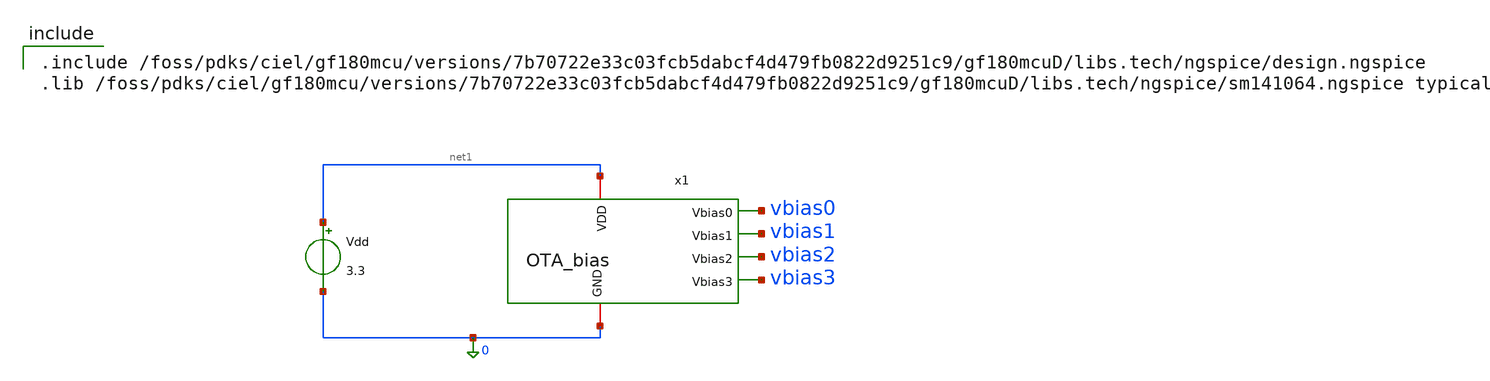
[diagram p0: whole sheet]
** sch_path: analog/tb_OTA_bias.sch
**.subckt tb_OTA_bias
x1 net1 vbias0 vbias2 vbias3 vbias1 0 OTA_bias cur_factor=1
Vdd net1 0 3.3
**** begin user architecture code

.include /foss/pdks/ciel/gf180mcu/versions/7b70722e33c03fcb5dabcf4d479fb0822d9251c9/gf180mcuD/libs.tech/ngspice/design.ngspice
.lib /foss/pdks/ciel/gf180mcu/versions/7b70722e33c03fcb5dabcf4d479fb0822d9251c9/gf180mcuD/libs.tech/ngspice/sm141064.ngspice typical



.control
alter @m.x1.x1.xm6.m0[w] = 10u

dc Vdd 0 3.3 0.05

plot (v(vbias0) - v(vbias3)) v(vbias1) v(vbias2)
plot @m.x1.x1.x1.xm6.m0[id] @m.x1.x1.x1.xm7.m0[id]
plot @m.x1.x1.xm2.m0[id] @m.x1.x1.xm6.m0[id] @m.x1.x1.xm9.m0[id] @m.x1.x1.xm1.m0[id]
+ @m.x1.x1.xm5.m0[id] @m.x1.x1.xm3.m0[id]

op
print @m.x1.x1.xm2.m0[id]
print @m.x1.x1.xm6.m0[id]
print @m.x1.x1.xm9.m0[id]
print @m.x1.x1.xm1.m0[id]
print @m.x1.x1.xm5.m0[id]
print @m.x1.x1.xm3.m0[id]
.endc


**** end user architecture code
**.ends

* expanding   symbol:
*+  AURA-Event-Driven-Mixed-Signal-ASIC-for-Acoustic-Pattern-Detection/analog/OTA_bias.sym # of pins=6
** sym_path: analog/OTA_bias.sym
** sch_path: analog/OTA_bias.sch
.subckt OTA_bias VDD Vbias0 Vbias2 Vbias3 Vbias1 GND  cur_factor=1
*.iopin VDD
*.opin Vbias2
*.opin Vbias1
*.opin Vbias0
*.opin Vbias3
*.iopin GND
XM1 Vbias1 GND Vbias2 VDD pfet_03v3 L=4u W=5u nf=1 ad='int((nf+1)/2) * W/nf * 0.18u' as='int((nf+2)/2) * W/nf * 0.18u'
+ pd='2*int((nf+1)/2) * (W/nf + 0.18u)' ps='2*int((nf+2)/2) * (W/nf + 0.18u)' nrd='0.18u / W' nrs='0.18u / W'
+ sa=0 sb=0 sd=0 m=1
XM4 Vbias1 Vbias2 net1 GND nfet_03v3 L=4u W=1u nf=1 ad='int((nf+1)/2) * W/nf * 0.18u' as='int((nf+2)/2) * W/nf * 0.18u'
+ pd='2*int((nf+1)/2) * (W/nf + 0.18u)' ps='2*int((nf+2)/2) * (W/nf + 0.18u)' nrd='0.18u / W' nrs='0.18u / W'
+ sa=0 sb=0 sd=0 m=1
XM5 net1 Vbias1 GND GND nfet_03v3 L=4u W=1u nf=1 ad='int((nf+1)/2) * W/nf * 0.18u' as='int((nf+2)/2) * W/nf * 0.18u'
+ pd='2*int((nf+1)/2) * (W/nf + 0.18u)' ps='2*int((nf+2)/2) * (W/nf + 0.18u)' nrd='0.18u / W' nrs='0.18u / W'
+ sa=0 sb=0 sd=0 m=1
XM9 net2 Vbias3 Vbias0 VDD pfet_03v3 L=4u W=5u nf=1 ad='int((nf+1)/2) * W/nf * 0.18u' as='int((nf+2)/2) * W/nf * 0.18u'
+ pd='2*int((nf+1)/2) * (W/nf + 0.18u)' ps='2*int((nf+2)/2) * (W/nf + 0.18u)' nrd='0.18u / W' nrs='0.18u / W'
+ sa=0 sb=0 sd=0 m=1
XM10 VDD Vbias0 net2 VDD pfet_03v3 L=4u W=5u nf=1 ad='int((nf+1)/2) * W/nf * 0.18u' as='int((nf+2)/2) * W/nf * 0.18u'
+ pd='2*int((nf+1)/2) * (W/nf + 0.18u)' ps='2*int((nf+2)/2) * (W/nf + 0.18u)' nrd='0.18u / W' nrs='0.18u / W'
+ sa=0 sb=0 sd=0 m=1
XM6 Vbias3 VDD Vbias0 GND nfet_03v3 L=4u W=10u nf=1 ad='int((nf+1)/2) * W/nf * 0.18u' as='int((nf+2)/2) * W/nf * 0.18u'
+ pd='2*int((nf+1)/2) * (W/nf + 0.18u)' ps='2*int((nf+2)/2) * (W/nf + 0.18u)' nrd='0.18u / W' nrs='0.18u / W'
+ sa=0 sb=0 sd=0 m=1
x1 VDD net3 net4 GND beta_multiplier_reference cur_factor={cur_factor}
XM2 Vbias2 net3 VDD VDD pfet_03v3 L=4u W=10u nf=1 ad='int((nf+1)/2) * W/nf * 0.18u' as='int((nf+2)/2) * W/nf * 0.18u'
+ pd='2*int((nf+1)/2) * (W/nf + 0.18u)' ps='2*int((nf+2)/2) * (W/nf + 0.18u)' nrd='0.18u / W' nrs='0.18u / W'
+ sa=0 sb=0 sd=0 m=1
XM3 GND net4 Vbias3 GND nfet_03v3 L=4u W=10u nf=1 ad='int((nf+1)/2) * W/nf * 0.18u' as='int((nf+2)/2) * W/nf * 0.18u'
+ pd='2*int((nf+1)/2) * (W/nf + 0.18u)' ps='2*int((nf+2)/2) * (W/nf + 0.18u)' nrd='0.18u / W' nrs='0.18u / W'
+ sa=0 sb=0 sd=0 m=1
.ends


* expanding   symbol:
*+  AURA-Event-Driven-Mixed-Signal-ASIC-for-Acoustic-Pattern-Detection/analog/beta_multiplier_reference.sym # of pins=4
** sym_path: analog/beta_multiplier_reference.sym
** sch_path: analog/beta_multiplier_reference.sch
.subckt beta_multiplier_reference VDD VbiasP VbiasN GND  length=410u
*.iopin VDD
*.iopin GND
*.opin VbiasP
*.opin VbiasN
XM2 VbiasN VbiasP VDD VDD pfet_03v3 L=4u W=2u nf=1 ad='int((nf+1)/2) * W/nf * 0.18u' as='int((nf+2)/2) * W/nf * 0.18u'
+ pd='2*int((nf+1)/2) * (W/nf + 0.18u)' ps='2*int((nf+2)/2) * (W/nf + 0.18u)' nrd='0.18u / W' nrs='0.18u / W'
+ sa=0 sb=0 sd=0 m=1
XM3 net2 VbiasP VDD VDD pfet_03v3 L=4u W=2u nf=1 ad='int((nf+1)/2) * W/nf * 0.18u' as='int((nf+2)/2) * W/nf * 0.18u'
+ pd='2*int((nf+1)/2) * (W/nf + 0.18u)' ps='2*int((nf+2)/2) * (W/nf + 0.18u)' nrd='0.18u / W' nrs='0.18u / W'
+ sa=0 sb=0 sd=0 m=1
XM6 VbiasN VbiasN GND GND nfet_03v3 L=4u W=10u nf=1 ad='int((nf+1)/2) * W/nf * 0.18u' as='int((nf+2)/2) * W/nf * 0.18u'
+ pd='2*int((nf+1)/2) * (W/nf + 0.18u)' ps='2*int((nf+2)/2) * (W/nf + 0.18u)' nrd='0.18u / W' nrs='0.18u / W'
+ sa=0 sb=0 sd=0 m=1
XM7 net2 VbiasN net1 GND nfet_03v3 L=4u W=10u nf=1 ad='int((nf+1)/2) * W/nf * 0.18u' as='int((nf+2)/2) * W/nf * 0.18u'
+ pd='2*int((nf+1)/2) * (W/nf + 0.18u)' ps='2*int((nf+2)/2) * (W/nf + 0.18u)' nrd='0.18u / W' nrs='0.18u / W'
+ sa=0 sb=0 sd=0 m=4
x1 VDD VbiasP net2 VbiasN VbiasN GND diff_amp
XM1 net4 net4 VDD VDD pfet_03v3 L=40u W=0.22u nf=1 ad='int((nf+1)/2) * W/nf * 0.18u' as='int((nf+2)/2) * W/nf * 0.18u'
+ pd='2*int((nf+1)/2) * (W/nf + 0.18u)' ps='2*int((nf+2)/2) * (W/nf + 0.18u)' nrd='0.18u / W' nrs='0.18u / W'
+ sa=0 sb=0 sd=0 m=1
XM4 VbiasP net3 VbiasN GND nfet_03v3 L=1u W=1u nf=1 ad='int((nf+1)/2) * W/nf * 0.18u' as='int((nf+2)/2) * W/nf * 0.18u'
+ pd='2*int((nf+1)/2) * (W/nf + 0.18u)' ps='2*int((nf+2)/2) * (W/nf + 0.18u)' nrd='0.18u / W' nrs='0.18u / W'
+ sa=0 sb=0 sd=0 m=1
XM5 net3 VbiasN GND GND nfet_03v3 L=10u W=1u nf=1 ad='int((nf+1)/2) * W/nf * 0.18u' as='int((nf+2)/2) * W/nf * 0.18u'
+ pd='2*int((nf+1)/2) * (W/nf + 0.18u)' ps='2*int((nf+2)/2) * (W/nf + 0.18u)' nrd='0.18u / W' nrs='0.18u / W'
+ sa=0 sb=0 sd=0 m=1
XM8 net5 net5 net4 VDD pfet_03v3 L=40u W=0.22u nf=1 ad='int((nf+1)/2) * W/nf * 0.18u' as='int((nf+2)/2) * W/nf * 0.18u'
+ pd='2*int((nf+1)/2) * (W/nf + 0.18u)' ps='2*int((nf+2)/2) * (W/nf + 0.18u)' nrd='0.18u / W' nrs='0.18u / W'
+ sa=0 sb=0 sd=0 m=1
XM9 net3 net5 net5 VDD pfet_03v3 L=40u W=0.22u nf=1 ad='int((nf+1)/2) * W/nf * 0.18u' as='int((nf+2)/2) * W/nf * 0.18u'
+ pd='2*int((nf+1)/2) * (W/nf + 0.18u)' ps='2*int((nf+2)/2) * (W/nf + 0.18u)' nrd='0.18u / W' nrs='0.18u / W'
+ sa=0 sb=0 sd=0 m=1
XR2 GND net1 GND ppolyf_u_2k r_width=2u r_length={length} m=1
.ends


* expanding   symbol:  AURA/diff_amp.sym # of pins=6
** sym_path: analog/diff_amp.sym
** sch_path: analog/diff_amp.sch
.subckt diff_amp VDD Vo V+ V- Vbias VSS
*.iopin VDD
*.iopin VSS
*.ipin V+
*.ipin V-
*.opin Vo
*.ipin Vbias
XM1 net1 V+ net2 VSS nfet_03v3 L=0.28u W=0.22u nf=1 ad='int((nf+1)/2) * W/nf * 0.18u' as='int((nf+2)/2) * W/nf * 0.18u'
+ pd='2*int((nf+1)/2) * (W/nf + 0.18u)' ps='2*int((nf+2)/2) * (W/nf + 0.18u)' nrd='0.18u / W' nrs='0.18u / W'
+ sa=0 sb=0 sd=0 m=1
XM2 net2 Vbias VSS VSS nfet_03v3 L=0.28u W=0.22u nf=1 ad='int((nf+1)/2) * W/nf * 0.18u' as='int((nf+2)/2) * W/nf * 0.18u'
+ pd='2*int((nf+1)/2) * (W/nf + 0.18u)' ps='2*int((nf+2)/2) * (W/nf + 0.18u)' nrd='0.18u / W' nrs='0.18u / W'
+ sa=0 sb=0 sd=0 m=1
XM3 Vo V- net2 VSS nfet_03v3 L=0.28u W=0.22u nf=1 ad='int((nf+1)/2) * W/nf * 0.18u' as='int((nf+2)/2) * W/nf * 0.18u'
+ pd='2*int((nf+1)/2) * (W/nf + 0.18u)' ps='2*int((nf+2)/2) * (W/nf + 0.18u)' nrd='0.18u / W' nrs='0.18u / W'
+ sa=0 sb=0 sd=0 m=1
XM4 Vo net1 VDD VDD pfet_03v3 L=0.28u W=0.22u nf=1 ad='int((nf+1)/2) * W/nf * 0.18u' as='int((nf+2)/2) * W/nf * 0.18u'
+ pd='2*int((nf+1)/2) * (W/nf + 0.18u)' ps='2*int((nf+2)/2) * (W/nf + 0.18u)' nrd='0.18u / W' nrs='0.18u / W'
+ sa=0 sb=0 sd=0 m=1
XM5 net1 net1 VDD VDD pfet_03v3 L=0.28u W=0.22u nf=1 ad='int((nf+1)/2) * W/nf * 0.18u' as='int((nf+2)/2) * W/nf * 0.18u'
+ pd='2*int((nf+1)/2) * (W/nf + 0.18u)' ps='2*int((nf+2)/2) * (W/nf + 0.18u)' nrd='0.18u / W' nrs='0.18u / W'
+ sa=0 sb=0 sd=0 m=1
.ends

.end
